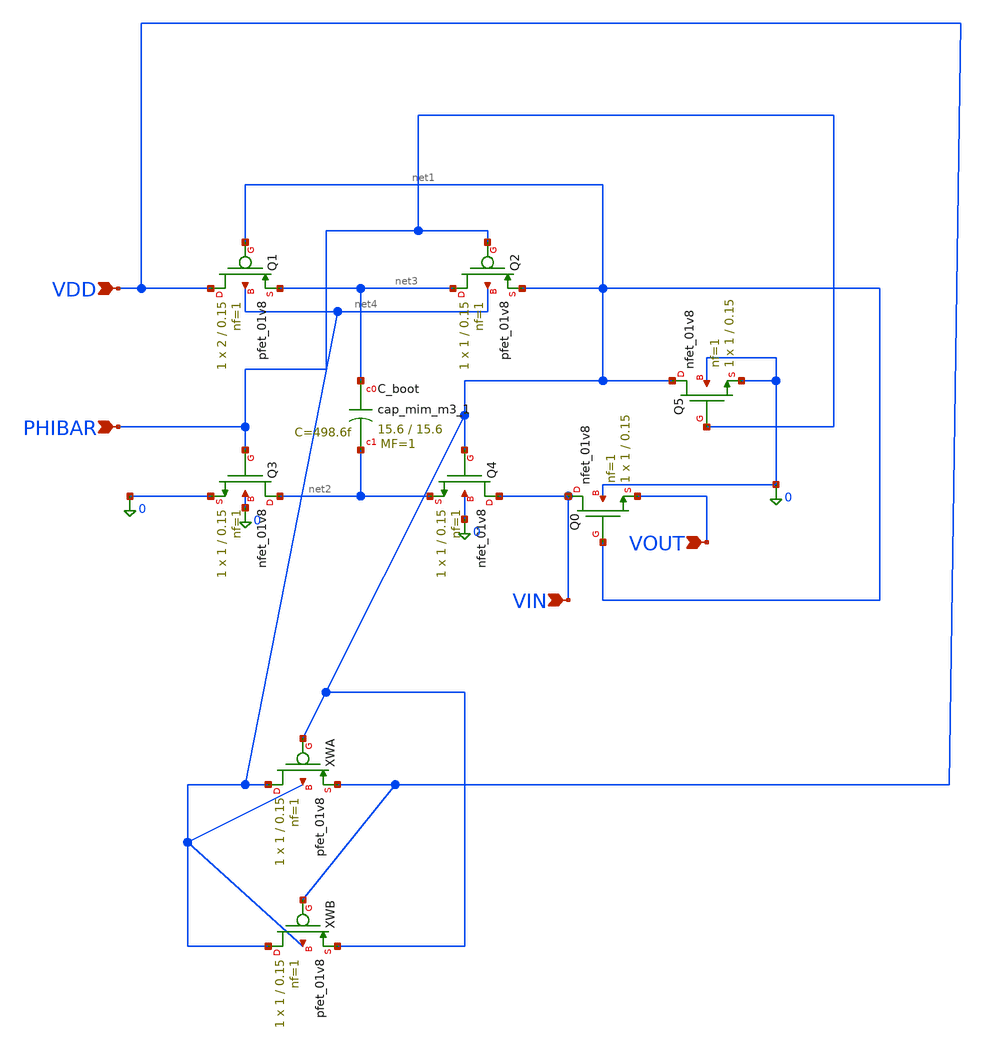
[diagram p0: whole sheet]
** sch_path: bootstrapped_switch.sch
**.subckt bootstrapped_switch VDD VIN VOUT PHIBAR
*.ipin VDD
*.ipin VIN
*.ipin VOUT
*.ipin PHIBAR
XQ0 VIN net1 VOUT 0 sky130_fd_pr__nfet_01v8 L=0.15 W=1 nf=1 ad='int((nf+1)/2) * W/nf * 0.29' as='int((nf+2)/2) * W/nf * 0.29'
+ pd='2*int((nf+1)/2) * (W/nf + 0.29)' ps='2*int((nf+2)/2) * (W/nf + 0.29)' nrd='0.29 / W' nrs='0.29 / W'
+ sa=0 sb=0 sd=0 mult=1 m=1
XC_boot net3 net2 sky130_fd_pr__cap_mim_m3_1 W=15.6 L=15.6 MF=1 m=1
XQ5 net1 PHIBAR 0 0 sky130_fd_pr__nfet_01v8 L=0.15 W=1 nf=1 ad='int((nf+1)/2) * W/nf * 0.29' as='int((nf+2)/2) * W/nf * 0.29'
+ pd='2*int((nf+1)/2) * (W/nf + 0.29)' ps='2*int((nf+2)/2) * (W/nf + 0.29)' nrd='0.29 / W' nrs='0.29 / W'
+ sa=0 sb=0 sd=0 mult=1 m=1
XQ4 VIN net1 net2 0 sky130_fd_pr__nfet_01v8 L=0.15 W=1 nf=1 ad='int((nf+1)/2) * W/nf * 0.29' as='int((nf+2)/2) * W/nf * 0.29'
+ pd='2*int((nf+1)/2) * (W/nf + 0.29)' ps='2*int((nf+2)/2) * (W/nf + 0.29)' nrd='0.29 / W' nrs='0.29 / W'
+ sa=0 sb=0 sd=0 mult=1 m=1
XQ1 VDD net1 net3 net4 sky130_fd_pr__pfet_01v8 L=0.15 W=2 nf=1 ad='int((nf+1)/2) * W/nf * 0.29' as='int((nf+2)/2) * W/nf * 0.29'
+ pd='2*int((nf+1)/2) * (W/nf + 0.29)' ps='2*int((nf+2)/2) * (W/nf + 0.29)' nrd='0.29 / W' nrs='0.29 / W'
+ sa=0 sb=0 sd=0 mult=1 m=1
XQ3 net2 PHIBAR 0 0 sky130_fd_pr__nfet_01v8 L=0.15 W=1 nf=1 ad='int((nf+1)/2) * W/nf * 0.29' as='int((nf+2)/2) * W/nf * 0.29'
+ pd='2*int((nf+1)/2) * (W/nf + 0.29)' ps='2*int((nf+2)/2) * (W/nf + 0.29)' nrd='0.29 / W' nrs='0.29 / W'
+ sa=0 sb=0 sd=0 mult=1 m=1
XQ2 net3 PHIBAR net1 net4 sky130_fd_pr__pfet_01v8 L=0.15 W=1 nf=1 ad='int((nf+1)/2) * W/nf * 0.29' as='int((nf+2)/2) * W/nf * 0.29'
+ pd='2*int((nf+1)/2) * (W/nf + 0.29)' ps='2*int((nf+2)/2) * (W/nf + 0.29)' nrd='0.29 / W' nrs='0.29 / W'
+ sa=0 sb=0 sd=0 mult=1 m=1
XXWA net4 net1 VDD net4 sky130_fd_pr__pfet_01v8 L=0.15 W=1 nf=1 ad='int((nf+1)/2) * W/nf * 0.29' as='int((nf+2)/2) * W/nf * 0.29'
+ pd='2*int((nf+1)/2) * (W/nf + 0.29)' ps='2*int((nf+2)/2) * (W/nf + 0.29)' nrd='0.29 / W' nrs='0.29 / W'
+ sa=0 sb=0 sd=0 mult=1 m=1
XXWB net4 VDD net1 net4 sky130_fd_pr__pfet_01v8 L=0.15 W=1 nf=1 ad='int((nf+1)/2) * W/nf * 0.29' as='int((nf+2)/2) * W/nf * 0.29'
+ pd='2*int((nf+1)/2) * (W/nf + 0.29)' ps='2*int((nf+2)/2) * (W/nf + 0.29)' nrd='0.29 / W' nrs='0.29 / W'
+ sa=0 sb=0 sd=0 mult=1 m=1
**.ends
.end
